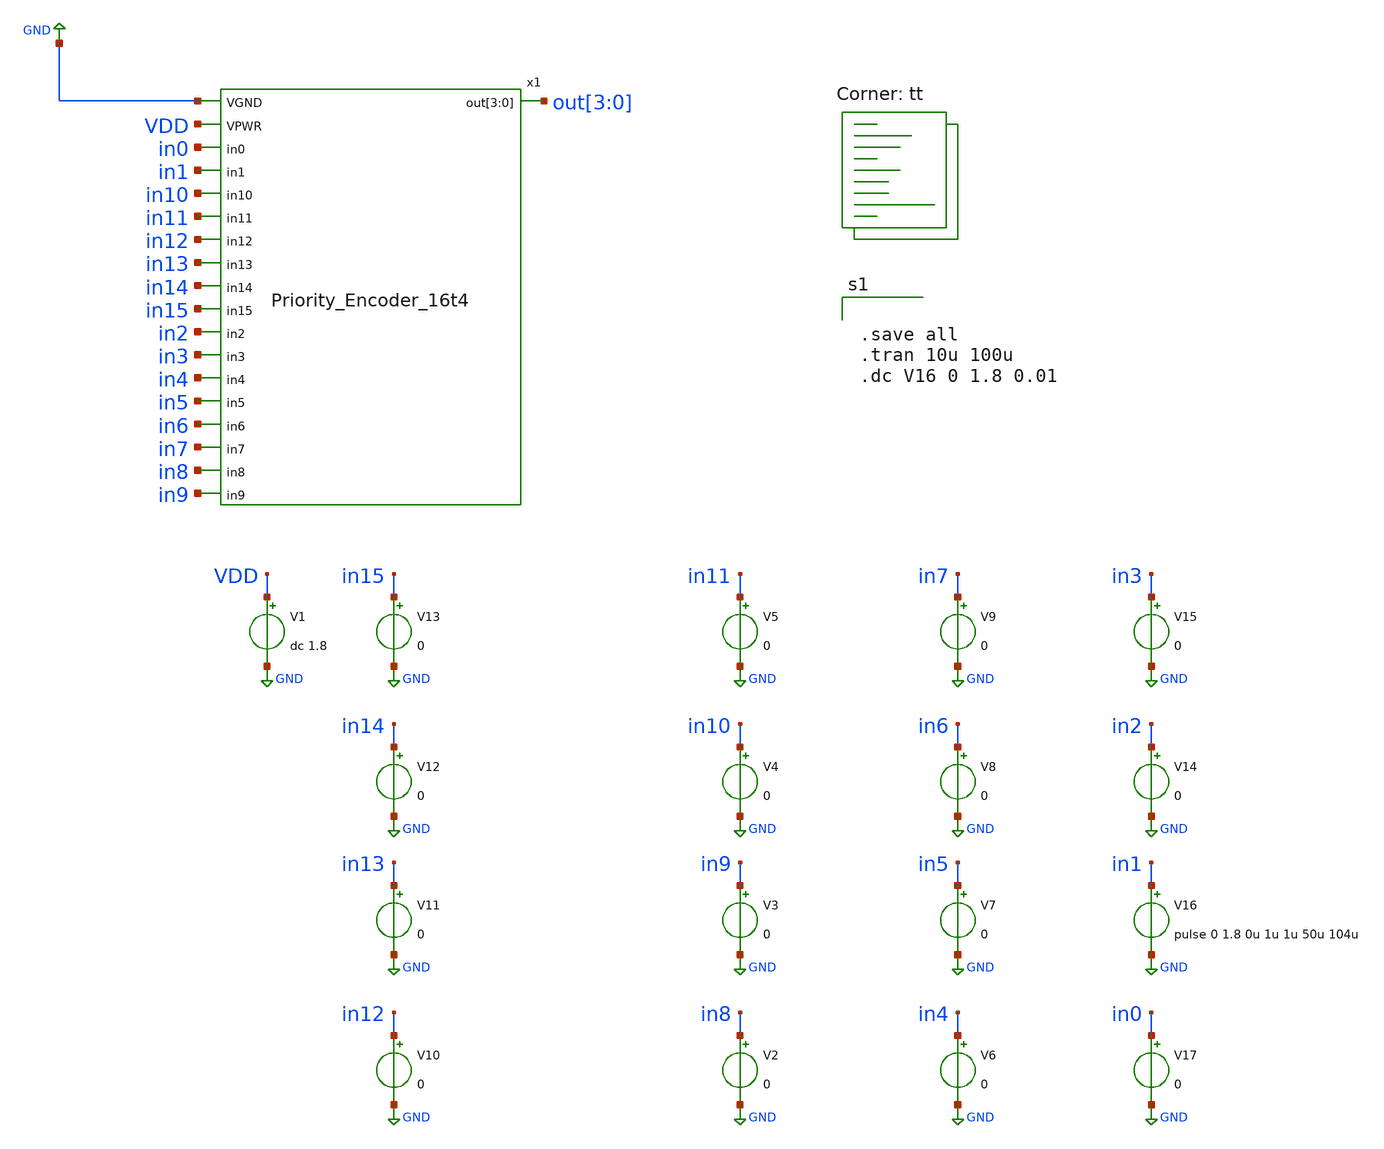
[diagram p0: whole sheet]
** sch_path: xschem/untitled.sch
**.subckt untitled
V1 VDD GND dc 1.8
V16 in1 GND pulse 0 1.8 0u 1u 1u 50u 104u
V17 in0 GND 0
x1 GND VDD in0 in1 in10 in11 in12 in13 in14 in15 in2 in3 in4 in5 in6 in7 in8 in9
+ Priority_Encoder_16t4
V2 in8 GND 0
V3 in9 GND 0
V4 in10 GND 0
V5 in11 GND 0
V6 in4 GND 0
V7 in5 GND 0
V8 in6 GND 0
V9 in7 GND 0
V10 in12 GND 0
V11 in13 GND 0
V12 in14 GND 0
V13 in15 GND 0
V14 in2 GND 0
V15 in3 GND 0
**** begin user architecture code
.lib $::SKYWATER_MODELS/sky130.lib.spice tt


.save all
.tran 10u 100u
.dc V16 0 1.8 0.01



** opencircuitdesign pdks install
.include $::SKYWATER_STDCELLS/sky130_fd_sc_hd.spice


**** end user architecture code
**.ends

* expanding   symbol:  Priority_Encoder_16t4.sym # of pins=19
** sym_path: xschem/to_send/Priority_Encoder_16t4.sym
** sch_path: xschem/to_send/Priority_Encoder_16t4.sch
.subckt Priority_Encoder_16t4 VGND VPWR in0 in1 in10 in11 in12 in13 in14 in15 in2 in3 in4 in5 in6
+ in7 in8 in9
*.ipin VGND
*.ipin VPWR
*.ipin in0
*.ipin in1
*.ipin in10
*.ipin in11
*.ipin in12
*.ipin in13
*.ipin in14
*.ipin in15
*.ipin in2
*.ipin in3
*.ipin in4
*.ipin in5
*.ipin in6
*.ipin in7
*.ipin in8
*.ipin in9
*.opin out[3],out[2],out[1],out[0]
X_16_ net8 VGND VGND VPWR VPWR _00_ sky130_fd_sc_hd__inv_2
X_17_ net1 _00_ net9 VGND VGND VPWR VPWR _01_ sky130_fd_sc_hd__a21oi_1
X_18_ net10 _01_ net11 VGND VGND VPWR VPWR _02_ sky130_fd_sc_hd__o21ba_1
X_19_ net12 _02_ net13 VGND VGND VPWR VPWR _03_ sky130_fd_sc_hd__o21ba_1
X_20_ net14 _03_ net15 VGND VGND VPWR VPWR _04_ sky130_fd_sc_hd__o21ba_1
X_21_ net2 _04_ net3 VGND VGND VPWR VPWR _05_ sky130_fd_sc_hd__o21ba_1
X_22_ net4 _05_ net5 VGND VGND VPWR VPWR _06_ sky130_fd_sc_hd__o21ba_1
X_23_ net6 _06_ net7 VGND VGND VPWR VPWR net16 sky130_fd_sc_hd__o21bai_4
X_24_ net10 net11 VGND VGND VPWR VPWR _07_ sky130_fd_sc_hd__nor2_1
X_25_ net8 net9 _07_ VGND VGND VPWR VPWR _08_ sky130_fd_sc_hd__o21a_1
X_26_ net14 net15 VGND VGND VPWR VPWR _09_ sky130_fd_sc_hd__nor2_1
X_27_ net12 net13 _08_ _09_ VGND VGND VPWR VPWR _10_ sky130_fd_sc_hd__o31a_1
X_28_ net2 net3 VGND VGND VPWR VPWR _11_ sky130_fd_sc_hd__nor2_1
X_29_ net4 net5 VGND VGND VPWR VPWR _12_ sky130_fd_sc_hd__nor2_1
X_30_ net2 net3 _10_ _12_ VGND VGND VPWR VPWR _13_ sky130_fd_sc_hd__o31a_1
X_31_ net6 net7 _13_ VGND VGND VPWR VPWR net17 sky130_fd_sc_hd__or3_2
X_32_ net4 net5 net6 net7 VGND VGND VPWR VPWR _14_ sky130_fd_sc_hd__or4_1
X_33_ net10 net11 net12 net13 VGND VGND VPWR VPWR _15_ sky130_fd_sc_hd__or4_1
X_34_ _09_ _11_ _15_ _14_ VGND VGND VPWR VPWR net18 sky130_fd_sc_hd__a31o_2
X_35_ net2 _14_ net3 _09_ VGND VGND VPWR VPWR net19 sky130_fd_sc_hd__or4b_4
Xinput1 in1 VGND VGND VPWR VPWR net1 sky130_fd_sc_hd__buf_2
Xinput10 in4 VGND VGND VPWR VPWR net10 sky130_fd_sc_hd__buf_2
Xinput11 in5 VGND VGND VPWR VPWR net11 sky130_fd_sc_hd__clkbuf_2
Xinput12 in6 VGND VGND VPWR VPWR net12 sky130_fd_sc_hd__clkbuf_2
Xinput13 in7 VGND VGND VPWR VPWR net13 sky130_fd_sc_hd__clkbuf_2
Xinput14 in8 VGND VGND VPWR VPWR net14 sky130_fd_sc_hd__clkbuf_2
Xinput15 in9 VGND VGND VPWR VPWR net15 sky130_fd_sc_hd__clkbuf_2
Xinput2 in10 VGND VGND VPWR VPWR net2 sky130_fd_sc_hd__clkbuf_2
Xinput3 in11 VGND VGND VPWR VPWR net3 sky130_fd_sc_hd__clkbuf_2
Xinput4 in12 VGND VGND VPWR VPWR net4 sky130_fd_sc_hd__buf_2
Xinput5 in13 VGND VGND VPWR VPWR net5 sky130_fd_sc_hd__buf_2
Xinput6 in14 VGND VGND VPWR VPWR net6 sky130_fd_sc_hd__buf_2
Xinput7 in15 VGND VGND VPWR VPWR net7 sky130_fd_sc_hd__dlymetal6s2s_1
Xinput8 in2 VGND VGND VPWR VPWR net8 sky130_fd_sc_hd__buf_2
Xinput9 in3 VGND VGND VPWR VPWR net9 sky130_fd_sc_hd__clkbuf_2
Xoutput16 net16 VGND VGND VPWR VPWR out[0] sky130_fd_sc_hd__buf_12
Xoutput17 net17 VGND VGND VPWR VPWR out[1] sky130_fd_sc_hd__buf_12
Xoutput18 net18 VGND VGND VPWR VPWR out[2] sky130_fd_sc_hd__buf_12
Xoutput19 net19 VGND VGND VPWR VPWR out[3] sky130_fd_sc_hd__buf_12
.ends

.GLOBAL GND
.end
